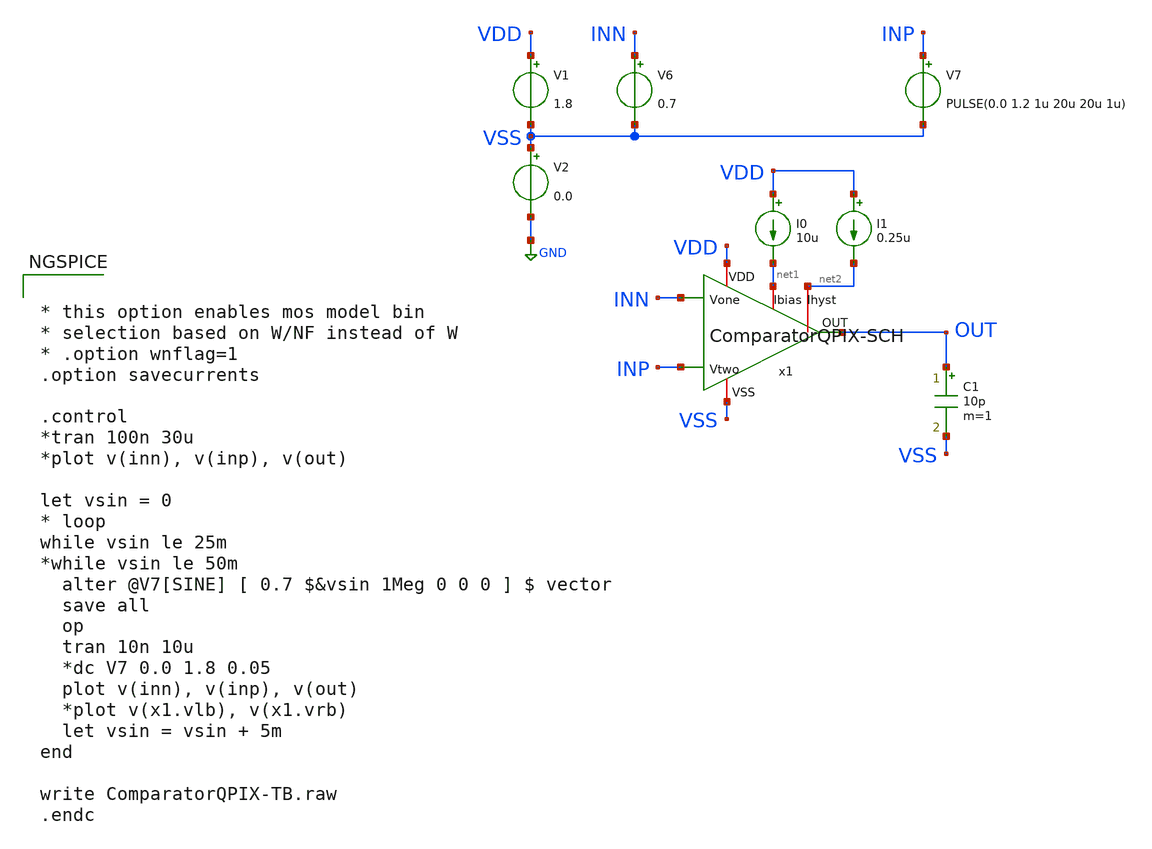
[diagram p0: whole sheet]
** sch_path: xschem/ComparatorQPIX-TB.sch
* YI/C9Shc8z/CWPKLJb8BQD+O4ziO4wpAwbu7u7s7HEAy2IIt2IIlQD6O4ziO4ypAAICtDl/GPL8AgNZy7Go7vwAAAAAAAAAAAAAAAAAAAAAAAPeMn2NHvywNosQhFFq
**.subckt ComparatorQPIX-TB
V1 VDD VSS 1.8
V2 VSS GND 0.0
V6 INN VSS 0.7
x1 VDD OUT VSS INN INP net1 net2 ComparatorQPIX-SCH
V7 INP VSS PULSE(0.0 1.2 1u 20u 20u 1u)
C1 OUT VSS 10p m=1
I0 VDD net1 10u
I1 VDD net2 0.25u
**** begin user architecture code

** opencircuitdesign pdks install
.lib $::SKYWATER_MODELS/sky130.lib.spice tt




* this option enables mos model bin
* selection based on W/NF instead of W
* .option wnflag=1
.option savecurrents

.control
*tran 100n 30u
*plot v(inn), v(inp), v(out)

let vsin = 0
* loop
while vsin le 25m
*while vsin le 50m
  alter @V7[SINE] [ 0.7 $&vsin 1Meg 0 0 0 ] $ vector
  save all
  op
  tran 10n 10u
  *dc V7 0.0 1.8 0.05
  plot v(inn), v(inp), v(out)
  *plot v(x1.vlb), v(x1.vrb)
  let vsin = vsin + 5m
end

write ComparatorQPIX-TB.raw
.endc


**** end user architecture code
**.ends
.GLOBAL GND
.end
